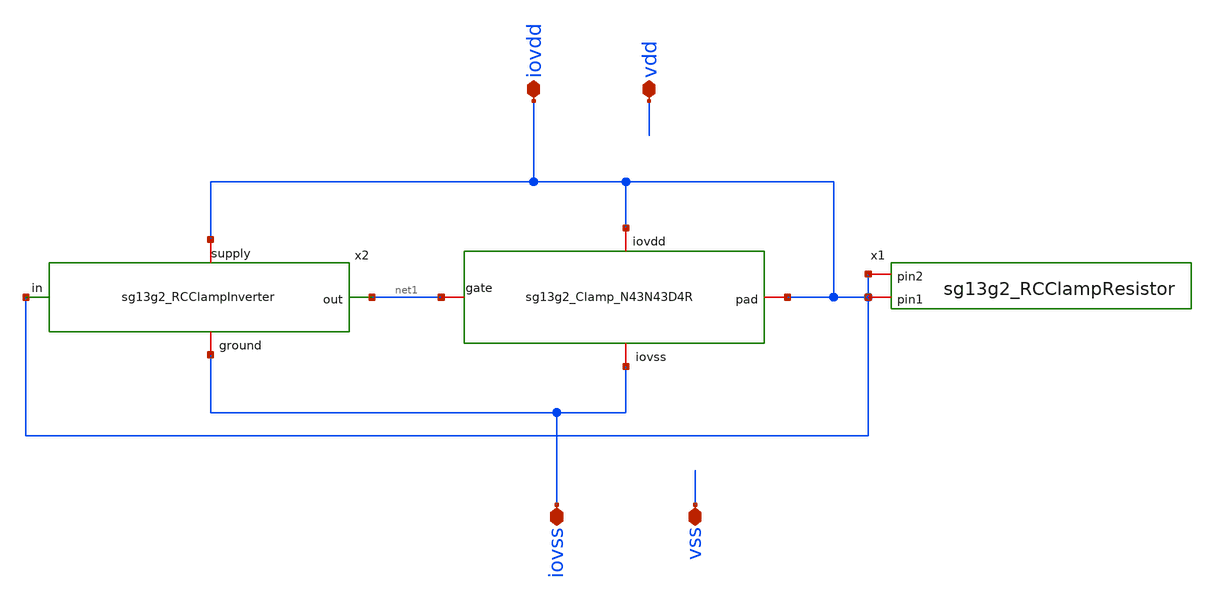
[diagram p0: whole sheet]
** sch_path: ihp-sg13g2/libs.ref/sg13g2_io/xschem/sg13g2_IOPadIOVdd.sch
**.subckt sg13g2_IOPadIOVdd iovss iovdd vss vdd
*.iopin iovss
*.iopin iovdd
*.iopin vss
*.iopin vdd
x1 iovdd iovdd sg13g2_RCClampResistor
x2 iovdd net1 iovdd iovss sg13g2_RCClampInverter
**.ends

* expanding   symbol:
*+  /home/prabhat.dubey/OPEN_Source_IHP_PDK/IHP-Open-PDK/ihp-sg13g2/libs.ref/sg13g2_io/xschem/sg13g2_RCClampResistor.sym # of pins=2
** sym_path: ihp-sg13g2/libs.ref/sg13g2_io/xschem/sg13g2_RCClampResistor.sym
** sch_path: ihp-sg13g2/libs.ref/sg13g2_io/xschem/sg13g2_RCClampResistor.sch
.subckt sg13g2_RCClampResistor pin2 pin1
*.iopin pin1
*.iopin pin2
XR1 net1 pin1 sub! rppd w=1.0e-6 l=20.0e-6 m=1 b=0 mm_ok=1
XR2 net2 net1 sub! rppd w=1.0e-6 l=20.0e-6 m=1 b=0 mm_ok=1
XR3 net3 net2 sub! rppd w=1.0e-6 l=20.0e-6 m=1 b=0 mm_ok=1
XR4 net4 net3 sub! rppd w=1.0e-6 l=20.0e-6 m=1 b=0 mm_ok=1
XR5 net7 net8 sub! rppd w=1.0e-6 l=20.0e-6 m=1 b=0 mm_ok=1
XR6 net6 net7 sub! rppd w=1.0e-6 l=20.0e-6 m=1 b=0 mm_ok=1
XR7 net5 net6 sub! rppd w=1.0e-6 l=20.0e-6 m=1 b=0 mm_ok=1
XR8 net4 net5 sub! rppd w=1.0e-6 l=20.0e-6 m=1 b=0 mm_ok=1
XR9 net9 net8 sub! rppd w=1.0e-6 l=20.0e-6 m=1 b=0 mm_ok=1
XR10 net10 net9 sub! rppd w=1.0e-6 l=20.0e-6 m=1 b=0 mm_ok=1
XR11 net11 net10 sub! rppd w=1.0e-6 l=20.0e-6 m=1 b=0 mm_ok=1
XR12 net12 net11 sub! rppd w=1.0e-6 l=20.0e-6 m=1 b=0 mm_ok=1
XR13 net15 net16 sub! rppd w=1.0e-6 l=20.0e-6 m=1 b=0 mm_ok=1
XR14 net14 net15 sub! rppd w=1.0e-6 l=20.0e-6 m=1 b=0 mm_ok=1
XR15 net13 net14 sub! rppd w=1.0e-6 l=20.0e-6 m=1 b=0 mm_ok=1
XR16 net12 net13 sub! rppd w=1.0e-6 l=20.0e-6 m=1 b=0 mm_ok=1
XR17 net17 net16 sub! rppd w=1.0e-6 l=20.0e-6 m=1 b=0 mm_ok=1
XR18 net18 net17 sub! rppd w=1.0e-6 l=20.0e-6 m=1 b=0 mm_ok=1
XR19 net19 net18 sub! rppd w=1.0e-6 l=20.0e-6 m=1 b=0 mm_ok=1
XR20 net20 net19 sub! rppd w=1.0e-6 l=20.0e-6 m=1 b=0 mm_ok=1
XR21 net23 net24 sub! rppd w=1.0e-6 l=20.0e-6 m=1 b=0 mm_ok=1
XR22 net22 net23 sub! rppd w=1.0e-6 l=20.0e-6 m=1 b=0 mm_ok=1
XR23 net21 net22 sub! rppd w=1.0e-6 l=20.0e-6 m=1 b=0 mm_ok=1
XR24 net20 net21 sub! rppd w=1.0e-6 l=20.0e-6 m=1 b=0 mm_ok=1
XR25 net25 net24 sub! rppd w=1.0e-6 l=20.0e-6 m=1 b=0 mm_ok=1
XR26 pin2 net25 sub! rppd w=1.0e-6 l=20.0e-6 m=1 b=0 mm_ok=1
.ends


* expanding   symbol:
*+  /home/prabhat.dubey/OPEN_Source_IHP_PDK/IHP-Open-PDK/ihp-sg13g2/libs.ref/sg13g2_io/xschem/sg13g2_RCClampInverter.sym # of pins=4
** sym_path: ihp-sg13g2/libs.ref/sg13g2_io/xschem/sg13g2_RCClampInverter.sym
** sch_path: ihp-sg13g2/libs.ref/sg13g2_io/xschem/sg13g2_RCClampInverter.sch
.subckt sg13g2_RCClampInverter supply out in ground
*.iopin supply
*.iopin ground
*.opin out
*.ipin in
XM1 ground in ground ground sg13_hv_nmos w=9.0u l=9.5u ng=1 m=1 mm_ok=1
XM2 ground in ground ground sg13_hv_nmos w=9.0u l=9.5u ng=1 m=1 mm_ok=1
XM3 ground in ground ground sg13_hv_nmos w=9.0u l=9.5u ng=1 m=1 mm_ok=1
XM4 ground in ground ground sg13_hv_nmos w=9.0u l=9.5u ng=1 m=1 mm_ok=1
XM5 ground in ground ground sg13_hv_nmos w=9.0u l=9.5u ng=1 m=1 mm_ok=1
XM6 ground in ground ground sg13_hv_nmos w=9.0u l=9.5u ng=1 m=1 mm_ok=1
XM7 ground in ground ground sg13_hv_nmos w=9.0u l=9.5u ng=1 m=1 mm_ok=1
XM8 ground in ground ground sg13_hv_nmos w=9.0u l=9.5u ng=1 m=1 mm_ok=1
XM9 ground in ground ground sg13_hv_nmos w=9.0u l=9.5u ng=1 m=1 mm_ok=1
XM10 ground in ground ground sg13_hv_nmos w=9.0u l=9.5u ng=1 m=1 mm_ok=1
XM11 ground in ground ground sg13_hv_nmos w=9.0u l=9.5u ng=1 m=1 mm_ok=1
XM12 ground in ground ground sg13_hv_nmos w=9.0u l=9.5u ng=1 m=1 mm_ok=1
XM13 ground in ground ground sg13_hv_nmos w=9.0u l=9.5u ng=1 m=1 mm_ok=1
XM14 ground in ground ground sg13_hv_nmos w=9.0u l=9.5u ng=1 m=1 mm_ok=1
XM15 out in ground ground sg13_hv_nmos w=9.0u l=0.5u ng=1 m=1 mm_ok=1
XM16 out in ground ground sg13_hv_nmos w=9.0u l=0.5u ng=1 m=1 mm_ok=1
XM17 out in ground ground sg13_hv_nmos w=9.0u l=0.5u ng=1 m=1 mm_ok=1
XM18 out in ground ground sg13_hv_nmos w=9.0u l=0.5u ng=1 m=1 mm_ok=1
XM19 out in ground ground sg13_hv_nmos w=9.0u l=0.5u ng=1 m=1 mm_ok=1
XM20 out in ground ground sg13_hv_nmos w=9.0u l=0.5u ng=1 m=1 mm_ok=1
XM21 out in ground ground sg13_hv_nmos w=9.0u l=0.5u ng=1 m=1 mm_ok=1
XM22 out in ground ground sg13_hv_nmos w=9.0u l=0.5u ng=1 m=1 mm_ok=1
XM23 out in ground ground sg13_hv_nmos w=9.0u l=0.5u ng=1 m=1 mm_ok=1
XM24 out in ground ground sg13_hv_nmos w=9.0u l=0.5u ng=1 m=1 mm_ok=1
XM25 out in ground ground sg13_hv_nmos w=9.0u l=0.5u ng=1 m=1 mm_ok=1
XM26 out in ground ground sg13_hv_nmos w=9.0u l=0.5u ng=1 m=1 mm_ok=1
XM27 out net1 supply supply sg13_hv_pmos w=7.0u l=0.5u ng=1 m=1 mm_ok=1
XM28 out net1 supply supply sg13_hv_pmos w=7.0u l=0.5u ng=1 m=1 mm_ok=1
XM29 out net1 supply supply sg13_hv_pmos w=7.0u l=0.5u ng=1 m=1 mm_ok=1
XM30 out net1 supply supply sg13_hv_pmos w=7.0u l=0.5u ng=1 m=1 mm_ok=1
XM31 out net1 supply supply sg13_hv_pmos w=7.0u l=0.5u ng=1 m=1 mm_ok=1
XM32 out net1 supply supply sg13_hv_pmos w=7.0u l=0.5u ng=1 m=1 mm_ok=1
XM33 out net1 supply supply sg13_hv_pmos w=7.0u l=0.5u ng=1 m=1 mm_ok=1
XM34 out net1 supply supply sg13_hv_pmos w=7.0u l=0.5u ng=1 m=1 mm_ok=1
XM35 out in supply supply sg13_hv_pmos w=7.0u l=0.5u ng=1 m=1 mm_ok=1
XM36 out net1 supply supply sg13_hv_pmos w=7.0u l=0.5u ng=1 m=1 mm_ok=1
XM37 out net1 supply supply sg13_hv_pmos w=7.0u l=0.5u ng=1 m=1 mm_ok=1
XM38 out net1 supply supply sg13_hv_pmos w=7.0u l=0.5u ng=1 m=1 mm_ok=1
XM39 out net1 supply supply sg13_hv_pmos w=7.0u l=0.5u ng=1 m=1 mm_ok=1
XM40 out net1 supply supply sg13_hv_pmos w=7.0u l=0.5u ng=1 m=1 mm_ok=1
XM41 out net1 supply supply sg13_hv_pmos w=7.0u l=0.5u ng=1 m=1 mm_ok=1
XM42 out net1 supply supply sg13_hv_pmos w=7.0u l=0.5u ng=1 m=1 mm_ok=1
XM43 out net1 supply supply sg13_hv_pmos w=7.0u l=0.5u ng=1 m=1 mm_ok=1
XM44 out net1 supply supply sg13_hv_pmos w=7.0u l=0.5u ng=1 m=1 mm_ok=1
XM45 out net1 supply supply sg13_hv_pmos w=7.0u l=0.5u ng=1 m=1 mm_ok=1
XM46 out net1 supply supply sg13_hv_pmos w=7.0u l=0.5u ng=1 m=1 mm_ok=1
XM47 out net1 supply supply sg13_hv_pmos w=7.0u l=0.5u ng=1 m=1 mm_ok=1
XM48 out net1 supply supply sg13_hv_pmos w=7.0u l=0.5u ng=1 m=1 mm_ok=1
XM49 out net1 supply supply sg13_hv_pmos w=7.0u l=0.5u ng=1 m=1 mm_ok=1
XM50 out net1 supply supply sg13_hv_pmos w=7.0u l=0.5u ng=1 m=1 mm_ok=1
XM51 out net1 supply supply sg13_hv_pmos w=7.0u l=0.5u ng=1 m=1 mm_ok=1
XM52 out in supply supply sg13_hv_pmos w=7.0u l=0.5u ng=1 m=1 mm_ok=1
XM53 out in supply supply sg13_hv_pmos w=7.0u l=0.5u ng=1 m=1 mm_ok=1
XM54 out in supply supply sg13_hv_pmos w=7.0u l=0.5u ng=1 m=1 mm_ok=1
XM55 out in supply supply sg13_hv_pmos w=7.0u l=0.5u ng=1 m=1 mm_ok=1
XM56 out in supply supply sg13_hv_pmos w=7.0u l=0.5u ng=1 m=1 mm_ok=1
XM57 out in supply supply sg13_hv_pmos w=7.0u l=0.5u ng=1 m=1 mm_ok=1
XM58 out in supply supply sg13_hv_pmos w=7.0u l=0.5u ng=1 m=1 mm_ok=1
XM59 out in supply supply sg13_hv_pmos w=7.0u l=0.5u ng=1 m=1 mm_ok=1
XM60 out in supply supply sg13_hv_pmos w=7.0u l=0.5u ng=1 m=1 mm_ok=1
XM61 out in supply supply sg13_hv_pmos w=7.0u l=0.5u ng=1 m=1 mm_ok=1
XM62 out in supply supply sg13_hv_pmos w=7.0u l=0.5u ng=1 m=1 mm_ok=1
XM63 out in supply supply sg13_hv_pmos w=7.0u l=0.5u ng=1 m=1 mm_ok=1
XM64 out in supply supply sg13_hv_pmos w=7.0u l=0.5u ng=1 m=1 mm_ok=1
XM65 out in supply supply sg13_hv_pmos w=7.0u l=0.5u ng=1 m=1 mm_ok=1
XM66 out in supply supply sg13_hv_pmos w=7.0u l=0.5u ng=1 m=1 mm_ok=1
XM67 out in supply supply sg13_hv_pmos w=7.0u l=0.5u ng=1 m=1 mm_ok=1
XM68 out in supply supply sg13_hv_pmos w=7.0u l=0.5u ng=1 m=1 mm_ok=1
XM69 out in supply supply sg13_hv_pmos w=7.0u l=0.5u ng=1 m=1 mm_ok=1
XM70 out in supply supply sg13_hv_pmos w=7.0u l=0.5u ng=1 m=1 mm_ok=1
XM71 out in supply supply sg13_hv_pmos w=7.0u l=0.5u ng=1 m=1 mm_ok=1
XM72 out in supply supply sg13_hv_pmos w=7.0u l=0.5u ng=1 m=1 mm_ok=1
XM73 out in supply supply sg13_hv_pmos w=7.0u l=0.5u ng=1 m=1 mm_ok=1
XM74 net2 in supply supply sg13_hv_pmos w=7.0u l=0.5u ng=1 m=1 mm_ok=1
XM75 out in supply supply sg13_hv_pmos w=7.0u l=0.5u ng=1 m=1 mm_ok=1
XM76 out in supply supply sg13_hv_pmos w=7.0u l=0.5u ng=1 m=1 mm_ok=1
.ends

.end
